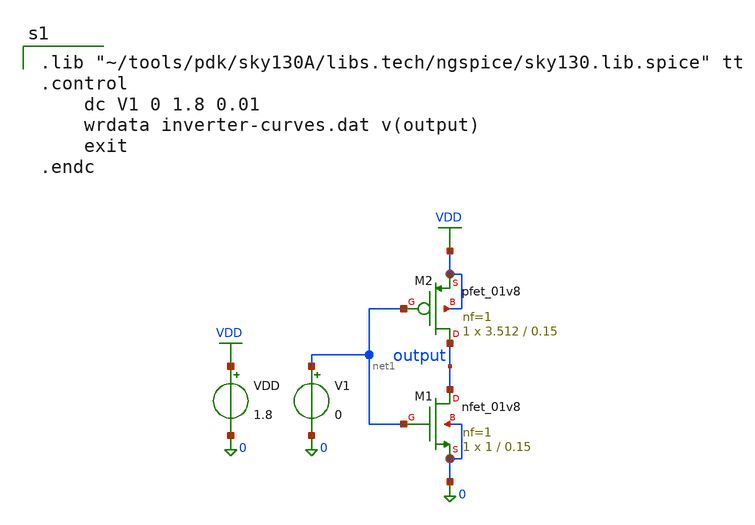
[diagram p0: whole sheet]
** sch_path: labs/cmos-inverter.sch
**.subckt cmos-inverter
XM1 output net1 0 0 sky130_fd_pr__nfet_01v8 L=0.15 W=1 nf=1 ad='int((nf+1)/2) * W/nf * 0.29' as='int((nf+2)/2) * W/nf * 0.29'
+ pd='2*int((nf+1)/2) * (W/nf + 0.29)' ps='2*int((nf+2)/2) * (W/nf + 0.29)' nrd='0.29 / W' nrs='0.29 / W'
+ sa=0 sb=0 sd=0 mult=1 m=1
XM2 output net1 VDD VDD sky130_fd_pr__pfet_01v8 L=0.15 W=3.512 nf=1 ad='int((nf+1)/2) * W/nf * 0.29'
+ as='int((nf+2)/2) * W/nf * 0.29' pd='2*int((nf+1)/2) * (W/nf + 0.29)' ps='2*int((nf+2)/2) * (W/nf + 0.29)'
+ nrd='0.29 / W' nrs='0.29 / W' sa=0 sb=0 sd=0 mult=1 m=1
V1 net1 0 0
VDD VDD 0 1.8
**** begin user architecture code

.lib "~/tools/pdk/sky130A/libs.tech/ngspice/sky130.lib.spice" tt
.control
    dc V1 0 1.8 0.01
    wrdata inverter-curves.dat v(output)
    exit
.endc

**** end user architecture code
**.ends
.GLOBAL VDD
.end
